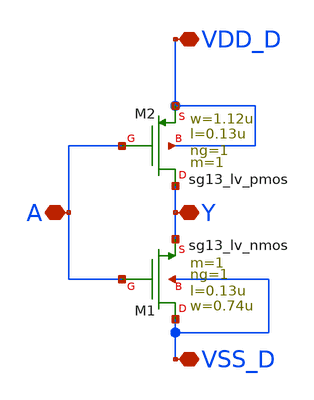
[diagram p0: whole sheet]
** sch_path: Python_layout/transmission_gate/inv_1_test.sch
**.subckt inv_1_test VDD_D VSS_D A Y
*.iopin VDD_D
*.iopin VSS_D
*.iopin A
*.iopin Y
XM1 VSS_D A Y VSS_D sg13_lv_nmos w=0.74u l=0.13u ng=1 m=1 mm_ok=1
XM2 Y A VDD_D VDD_D sg13_lv_pmos w=1.12u l=0.13u ng=1 m=1 mm_ok=1
**.ends
.end
